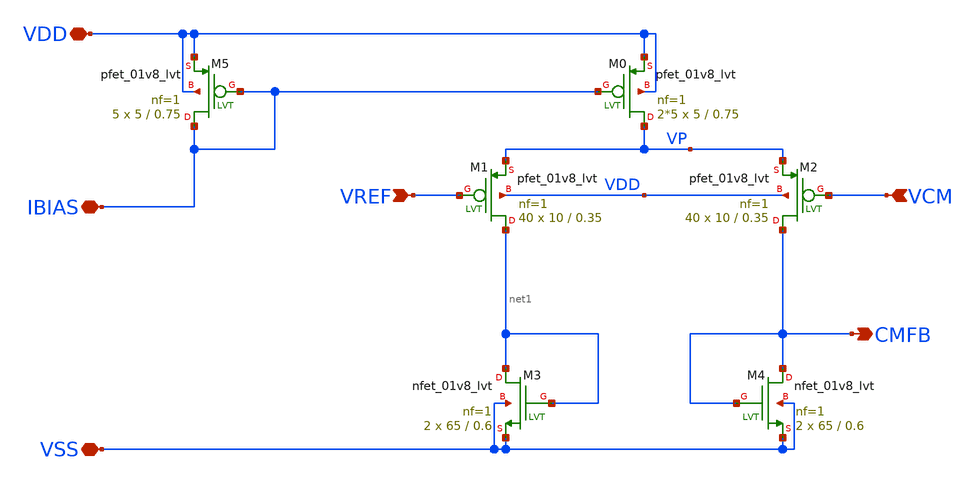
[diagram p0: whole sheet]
** sch_path: Differential_OTA_Telescopic_IHP/OTA_Telescopic_CMFB_v2.sch
**.subckt OTA_Telescopic_CMFB_v2 VDD IBIAS VSS VREF VCM CMFB
*.iopin VDD
*.iopin IBIAS
*.iopin VSS
*.ipin VREF
*.ipin VCM
*.opin CMFB
XM0 VP IBIAS VDD VDD sky130_fd_pr__pfet_01v8_lvt L=0.75 W=5 nf=1 ad='int((nf+1)/2) * W/nf * 0.29' as='int((nf+2)/2) * W/nf * 0.29'
+ pd='2*int((nf+1)/2) * (W/nf + 0.29)' ps='2*int((nf+2)/2) * (W/nf + 0.29)' nrd='0.29 / W' nrs='0.29 / W'
+ sa=0 sb=0 sd=0 mult=2*5 m=2*5
XM1 net1 VREF VP VDD sky130_fd_pr__pfet_01v8_lvt L=0.35 W=10 nf=1 ad='int((nf+1)/2) * W/nf * 0.29' as='int((nf+2)/2) * W/nf * 0.29'
+ pd='2*int((nf+1)/2) * (W/nf + 0.29)' ps='2*int((nf+2)/2) * (W/nf + 0.29)' nrd='0.29 / W' nrs='0.29 / W'
+ sa=0 sb=0 sd=0 mult=40 m=40
XM2 CMFB VCM VP VDD sky130_fd_pr__pfet_01v8_lvt L=0.35 W=10 nf=1 ad='int((nf+1)/2) * W/nf * 0.29' as='int((nf+2)/2) * W/nf * 0.29'
+ pd='2*int((nf+1)/2) * (W/nf + 0.29)' ps='2*int((nf+2)/2) * (W/nf + 0.29)' nrd='0.29 / W' nrs='0.29 / W'
+ sa=0 sb=0 sd=0 mult=40 m=40
XM5 IBIAS IBIAS VDD VDD sky130_fd_pr__pfet_01v8_lvt L=0.75 W=5 nf=1 ad='int((nf+1)/2) * W/nf * 0.29'
+ as='int((nf+2)/2) * W/nf * 0.29' pd='2*int((nf+1)/2) * (W/nf + 0.29)' ps='2*int((nf+2)/2) * (W/nf + 0.29)'
+ nrd='0.29 / W' nrs='0.29 / W' sa=0 sb=0 sd=0 mult=5 m=5
XM3 net1 net1 VSS VSS sky130_fd_pr__nfet_01v8_lvt L=0.6 W=65 nf=1 ad='int((nf+1)/2) * W/nf * 0.29' as='int((nf+2)/2) * W/nf * 0.29'
+ pd='2*int((nf+1)/2) * (W/nf + 0.29)' ps='2*int((nf+2)/2) * (W/nf + 0.29)' nrd='0.29 / W' nrs='0.29 / W'
+ sa=0 sb=0 sd=0 mult=2 m=2
XM4 CMFB CMFB VSS VSS sky130_fd_pr__nfet_01v8_lvt L=0.6 W=65 nf=1 ad='int((nf+1)/2) * W/nf * 0.29' as='int((nf+2)/2) * W/nf * 0.29'
+ pd='2*int((nf+1)/2) * (W/nf + 0.29)' ps='2*int((nf+2)/2) * (W/nf + 0.29)' nrd='0.29 / W' nrs='0.29 / W'
+ sa=0 sb=0 sd=0 mult=2 m=2
**.ends
.end
